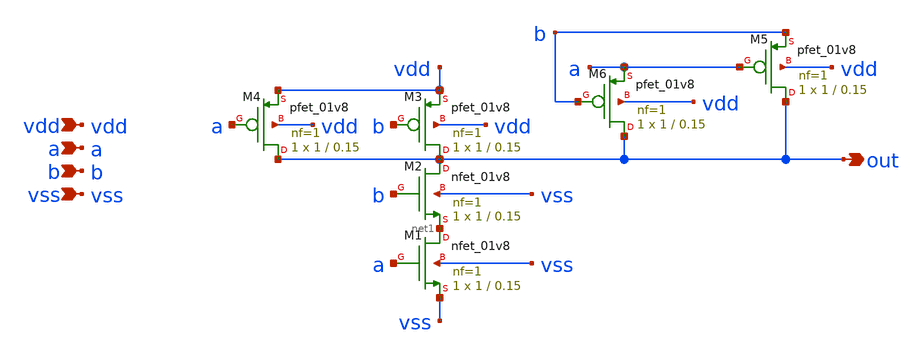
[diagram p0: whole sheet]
** sch_path: custom_gds/tt_um_tim2305_adc_dac/xschem/tnand.sch
**.subckt tnand vdd a b vss out
*.ipin vdd
*.ipin a
*.ipin b
*.ipin vss
*.opin out
XM1 net1 a vss vss sky130_fd_pr__nfet_01v8 L=0.15 W=1 nf=1 ad='int((nf+1)/2) * W/nf * 0.29' as='int((nf+2)/2) * W/nf * 0.29'
+ pd='2*int((nf+1)/2) * (W/nf + 0.29)' ps='2*int((nf+2)/2) * (W/nf + 0.29)' nrd='0.29 / W' nrs='0.29 / W'
+ sa=0 sb=0 sd=0 mult=1 m=1
XM2 out b net1 vss sky130_fd_pr__nfet_01v8 L=0.15 W=1 nf=1 ad='int((nf+1)/2) * W/nf * 0.29' as='int((nf+2)/2) * W/nf * 0.29'
+ pd='2*int((nf+1)/2) * (W/nf + 0.29)' ps='2*int((nf+2)/2) * (W/nf + 0.29)' nrd='0.29 / W' nrs='0.29 / W'
+ sa=0 sb=0 sd=0 mult=1 m=1
XM3 out b vdd vdd sky130_fd_pr__pfet_01v8 L=0.15 W=1 nf=1 ad='int((nf+1)/2) * W/nf * 0.29' as='int((nf+2)/2) * W/nf * 0.29'
+ pd='2*int((nf+1)/2) * (W/nf + 0.29)' ps='2*int((nf+2)/2) * (W/nf + 0.29)' nrd='0.29 / W' nrs='0.29 / W'
+ sa=0 sb=0 sd=0 mult=1 m=1
XM4 out a vdd vdd sky130_fd_pr__pfet_01v8 L=0.15 W=1 nf=1 ad='int((nf+1)/2) * W/nf * 0.29' as='int((nf+2)/2) * W/nf * 0.29'
+ pd='2*int((nf+1)/2) * (W/nf + 0.29)' ps='2*int((nf+2)/2) * (W/nf + 0.29)' nrd='0.29 / W' nrs='0.29 / W'
+ sa=0 sb=0 sd=0 mult=1 m=1
XM5 out a b vdd sky130_fd_pr__pfet_01v8 L=0.15 W=1 nf=1 ad='int((nf+1)/2) * W/nf * 0.29' as='int((nf+2)/2) * W/nf * 0.29'
+ pd='2*int((nf+1)/2) * (W/nf + 0.29)' ps='2*int((nf+2)/2) * (W/nf + 0.29)' nrd='0.29 / W' nrs='0.29 / W'
+ sa=0 sb=0 sd=0 mult=1 m=1
XM6 out b a vdd sky130_fd_pr__pfet_01v8 L=0.15 W=1 nf=1 ad='int((nf+1)/2) * W/nf * 0.29' as='int((nf+2)/2) * W/nf * 0.29'
+ pd='2*int((nf+1)/2) * (W/nf + 0.29)' ps='2*int((nf+2)/2) * (W/nf + 0.29)' nrd='0.29 / W' nrs='0.29 / W'
+ sa=0 sb=0 sd=0 mult=1 m=1
**.ends
.end
